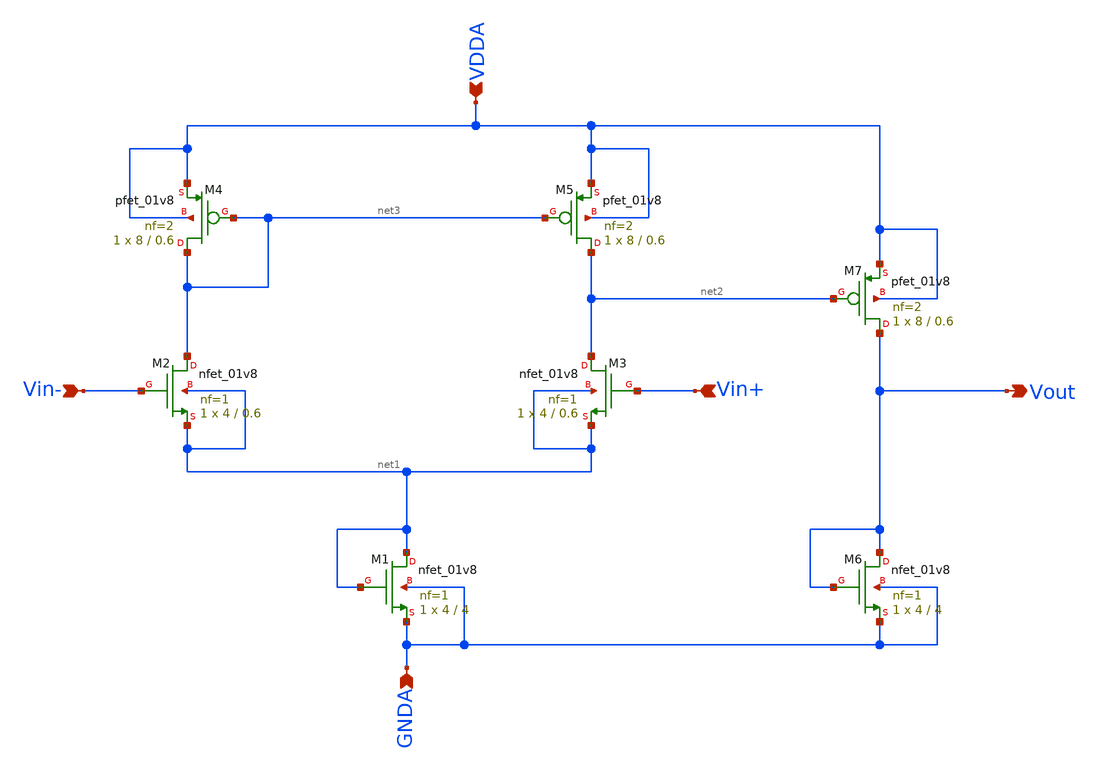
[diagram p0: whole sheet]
** sch_path: projects/bandgapref/xschem_ngspice/new_files/opamp_bandgap_2.sch
**.subckt opamp_bandgap_2 Vin+ Vout Vin- GNDA VDDA
*.ipin Vin+
*.opin Vout
*.ipin Vin-
*.ipin GNDA
*.ipin VDDA
XM1 net1 net1 GNDA GNDA sky130_fd_pr__nfet_01v8 L=4 W=4 nf=1 ad='int((nf+1)/2) * W/nf * 0.29' as='int((nf+2)/2) * W/nf * 0.29'
+ pd='2*int((nf+1)/2) * (W/nf + 0.29)' ps='2*int((nf+2)/2) * (W/nf + 0.29)' nrd='0.29 / W' nrs='0.29 / W'
+ sa=0 sb=0 sd=0 mult=1 m=1
XM2 net3 Vin- net1 net1 sky130_fd_pr__nfet_01v8 L=0.6 W=4 nf=1 ad='int((nf+1)/2) * W/nf * 0.29' as='int((nf+2)/2) * W/nf * 0.29'
+ pd='2*int((nf+1)/2) * (W/nf + 0.29)' ps='2*int((nf+2)/2) * (W/nf + 0.29)' nrd='0.29 / W' nrs='0.29 / W'
+ sa=0 sb=0 sd=0 mult=1 m=1
XM3 net2 Vin+ net1 net1 sky130_fd_pr__nfet_01v8 L=0.6 W=4 nf=1 ad='int((nf+1)/2) * W/nf * 0.29' as='int((nf+2)/2) * W/nf * 0.29'
+ pd='2*int((nf+1)/2) * (W/nf + 0.29)' ps='2*int((nf+2)/2) * (W/nf + 0.29)' nrd='0.29 / W' nrs='0.29 / W'
+ sa=0 sb=0 sd=0 mult=1 m=1
XM4 net3 net3 VDDA VDDA sky130_fd_pr__pfet_01v8 L=0.6 W=8 nf=2 ad='int((nf+1)/2) * W/nf * 0.29' as='int((nf+2)/2) * W/nf * 0.29'
+ pd='2*int((nf+1)/2) * (W/nf + 0.29)' ps='2*int((nf+2)/2) * (W/nf + 0.29)' nrd='0.29 / W' nrs='0.29 / W'
+ sa=0 sb=0 sd=0 mult=1 m=1
XM5 net2 net3 VDDA VDDA sky130_fd_pr__pfet_01v8 L=0.6 W=8 nf=2 ad='int((nf+1)/2) * W/nf * 0.29' as='int((nf+2)/2) * W/nf * 0.29'
+ pd='2*int((nf+1)/2) * (W/nf + 0.29)' ps='2*int((nf+2)/2) * (W/nf + 0.29)' nrd='0.29 / W' nrs='0.29 / W'
+ sa=0 sb=0 sd=0 mult=1 m=1
XM6 Vout Vout GNDA GNDA sky130_fd_pr__nfet_01v8 L=4 W=4 nf=1 ad='int((nf+1)/2) * W/nf * 0.29' as='int((nf+2)/2) * W/nf * 0.29'
+ pd='2*int((nf+1)/2) * (W/nf + 0.29)' ps='2*int((nf+2)/2) * (W/nf + 0.29)' nrd='0.29 / W' nrs='0.29 / W'
+ sa=0 sb=0 sd=0 mult=1 m=1
XM7 Vout net2 VDDA VDDA sky130_fd_pr__pfet_01v8 L=0.6 W=8 nf=2 ad='int((nf+1)/2) * W/nf * 0.29' as='int((nf+2)/2) * W/nf * 0.29'
+ pd='2*int((nf+1)/2) * (W/nf + 0.29)' ps='2*int((nf+2)/2) * (W/nf + 0.29)' nrd='0.29 / W' nrs='0.29 / W'
+ sa=0 sb=0 sd=0 mult=1 m=1
**.ends
.end
